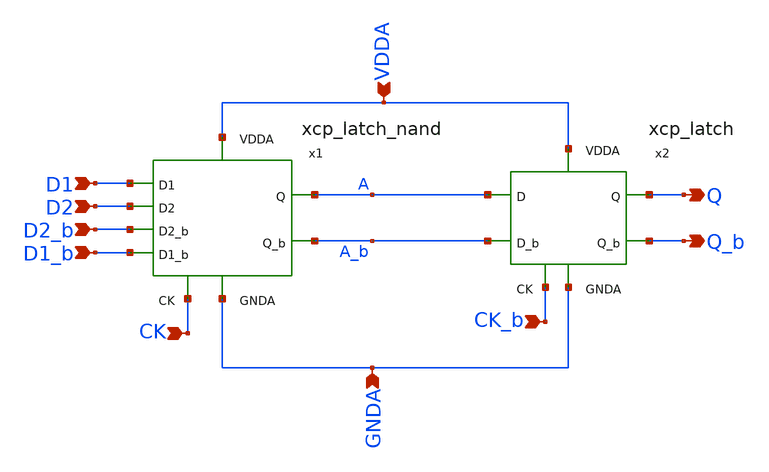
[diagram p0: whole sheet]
** sch_path: projects/pll/divider/xschem_ngspice/xcp_FF_nand.sch
**.subckt xcp_FF_nand VDDA Q CK GNDA D2 Q_b CK_b D2_b D1 D1_b
*.ipin VDDA
*.opin Q
*.ipin CK
*.ipin GNDA
*.ipin D2
*.opin Q_b
*.ipin CK_b
*.ipin D2_b
*.ipin D1
*.ipin D1_b
x2 VDDA Q_b Q A_b A CK_b GNDA xcp_latch
x1 VDDA A_b A D1 D1_b D2_b D2 CK GNDA xcp_latch_nand
**.ends

* expanding   symbol:  /foss/designs/my_design/projects/pll/divider/xschem_ngspice/xcp_latch.sym #
*+ of pins=7
** sym_path: projects/pll/divider/xschem_ngspice/xcp_latch.sym
** sch_path: projects/pll/divider/xschem_ngspice/xcp_latch.sch
.subckt xcp_latch VDDA Q_b Q D_b D CK GNDA
*.ipin D
*.opin Q
*.ipin D_b
*.ipin CK
*.opin Q_b
*.ipin VDDA
*.ipin GNDA
XM5 net1 CK GNDA GNDA sky130_fd_pr__nfet_01v8 L=0.15 W=2 nf=2 ad='int((nf+1)/2) * W/nf * 0.29' as='int((nf+2)/2) * W/nf * 0.29'
+ pd='2*int((nf+1)/2) * (W/nf + 0.29)' ps='2*int((nf+2)/2) * (W/nf + 0.29)' nrd='0.29 / W' nrs='0.29 / W'
+ sa=0 sb=0 sd=0 mult=1 m=1
XM1 net3 D V_common GNDA sky130_fd_pr__nfet_01v8 L=0.15 W=1 nf=1 ad='int((nf+1)/2) * W/nf * 0.29' as='int((nf+2)/2) * W/nf * 0.29'
+ pd='2*int((nf+1)/2) * (W/nf + 0.29)' ps='2*int((nf+2)/2) * (W/nf + 0.29)' nrd='0.29 / W' nrs='0.29 / W'
+ sa=0 sb=0 sd=0 mult=1 m=1
XM2 net2 D_b V_common GNDA sky130_fd_pr__nfet_01v8 L=0.15 W=1 nf=1 ad='int((nf+1)/2) * W/nf * 0.29' as='int((nf+2)/2) * W/nf * 0.29'
+ pd='2*int((nf+1)/2) * (W/nf + 0.29)' ps='2*int((nf+2)/2) * (W/nf + 0.29)' nrd='0.29 / W' nrs='0.29 / W'
+ sa=0 sb=0 sd=0 mult=1 m=1
Vmeas V_common net1 0
.save i(vmeas)
Vmeas1 Q_b net3 0
.save i(vmeas1)
Vmeas2 Q net2 0
.save i(vmeas2)
XM3 Q_b Q VDDA VDDA sky130_fd_pr__pfet_01v8 L=0.15 W=1 nf=1 ad='int((nf+1)/2) * W/nf * 0.29' as='int((nf+2)/2) * W/nf * 0.29'
+ pd='2*int((nf+1)/2) * (W/nf + 0.29)' ps='2*int((nf+2)/2) * (W/nf + 0.29)' nrd='0.29 / W' nrs='0.29 / W'
+ sa=0 sb=0 sd=0 mult=1 m=1
XM4 Q Q_b VDDA VDDA sky130_fd_pr__pfet_01v8 L=0.15 W=1 nf=1 ad='int((nf+1)/2) * W/nf * 0.29' as='int((nf+2)/2) * W/nf * 0.29'
+ pd='2*int((nf+1)/2) * (W/nf + 0.29)' ps='2*int((nf+2)/2) * (W/nf + 0.29)' nrd='0.29 / W' nrs='0.29 / W'
+ sa=0 sb=0 sd=0 mult=1 m=1
.ends


* expanding   symbol:
*+  /foss/designs/my_design/projects/pll/divider/xschem_ngspice/xcp_latch_nand.sym # of pins=9
** sym_path: projects/pll/divider/xschem_ngspice/xcp_latch_nand.sym
** sch_path: projects/pll/divider/xschem_ngspice/xcp_latch_nand.sch
.subckt xcp_latch_nand VDDA Q_b Q D1 D1_b D2_b D2 CK GNDA
*.ipin D2
*.opin Q
*.ipin D1_b
*.ipin CK
*.opin Q_b
*.ipin VDDA
*.ipin GNDA
*.ipin D1
*.ipin D2_b
XM5 net1 CK GNDA GNDA sky130_fd_pr__nfet_01v8 L=0.15 W=2 nf=2 ad='int((nf+1)/2) * W/nf * 0.29' as='int((nf+2)/2) * W/nf * 0.29'
+ pd='2*int((nf+1)/2) * (W/nf + 0.29)' ps='2*int((nf+2)/2) * (W/nf + 0.29)' nrd='0.29 / W' nrs='0.29 / W'
+ sa=0 sb=0 sd=0 mult=1 m=1
XM1 net4 D2 V_common GNDA sky130_fd_pr__nfet_01v8 L=0.15 W=1 nf=1 ad='int((nf+1)/2) * W/nf * 0.29' as='int((nf+2)/2) * W/nf * 0.29'
+ pd='2*int((nf+1)/2) * (W/nf + 0.29)' ps='2*int((nf+2)/2) * (W/nf + 0.29)' nrd='0.29 / W' nrs='0.29 / W'
+ sa=0 sb=0 sd=0 mult=1 m=1
XM2 net2 D1_b V_common GNDA sky130_fd_pr__nfet_01v8 L=0.15 W=1 nf=1 ad='int((nf+1)/2) * W/nf * 0.29'
+ as='int((nf+2)/2) * W/nf * 0.29' pd='2*int((nf+1)/2) * (W/nf + 0.29)' ps='2*int((nf+2)/2) * (W/nf + 0.29)'
+ nrd='0.29 / W' nrs='0.29 / W' sa=0 sb=0 sd=0 mult=1 m=1
Vmeas V_common net1 0
.save i(vmeas)
Vmeas1 Q_b net3 0
.save i(vmeas1)
Vmeas2 Q net2 0
.save i(vmeas2)
XM3 Q_b Q VDDA VDDA sky130_fd_pr__pfet_01v8 L=0.15 W=1 nf=1 ad='int((nf+1)/2) * W/nf * 0.29' as='int((nf+2)/2) * W/nf * 0.29'
+ pd='2*int((nf+1)/2) * (W/nf + 0.29)' ps='2*int((nf+2)/2) * (W/nf + 0.29)' nrd='0.29 / W' nrs='0.29 / W'
+ sa=0 sb=0 sd=0 mult=1 m=1
XM4 Q Q_b VDDA VDDA sky130_fd_pr__pfet_01v8 L=0.15 W=1 nf=1 ad='int((nf+1)/2) * W/nf * 0.29' as='int((nf+2)/2) * W/nf * 0.29'
+ pd='2*int((nf+1)/2) * (W/nf + 0.29)' ps='2*int((nf+2)/2) * (W/nf + 0.29)' nrd='0.29 / W' nrs='0.29 / W'
+ sa=0 sb=0 sd=0 mult=1 m=1
XM6 net3 D1 net4 GNDA sky130_fd_pr__nfet_01v8 L=0.15 W=1 nf=1 ad='int((nf+1)/2) * W/nf * 0.29' as='int((nf+2)/2) * W/nf * 0.29'
+ pd='2*int((nf+1)/2) * (W/nf + 0.29)' ps='2*int((nf+2)/2) * (W/nf + 0.29)' nrd='0.29 / W' nrs='0.29 / W'
+ sa=0 sb=0 sd=0 mult=1 m=1
XM7 net2 D2_b V_common GNDA sky130_fd_pr__nfet_01v8 L=0.15 W=1 nf=1 ad='int((nf+1)/2) * W/nf * 0.29'
+ as='int((nf+2)/2) * W/nf * 0.29' pd='2*int((nf+1)/2) * (W/nf + 0.29)' ps='2*int((nf+2)/2) * (W/nf + 0.29)'
+ nrd='0.29 / W' nrs='0.29 / W' sa=0 sb=0 sd=0 mult=1 m=1
.ends

.end
